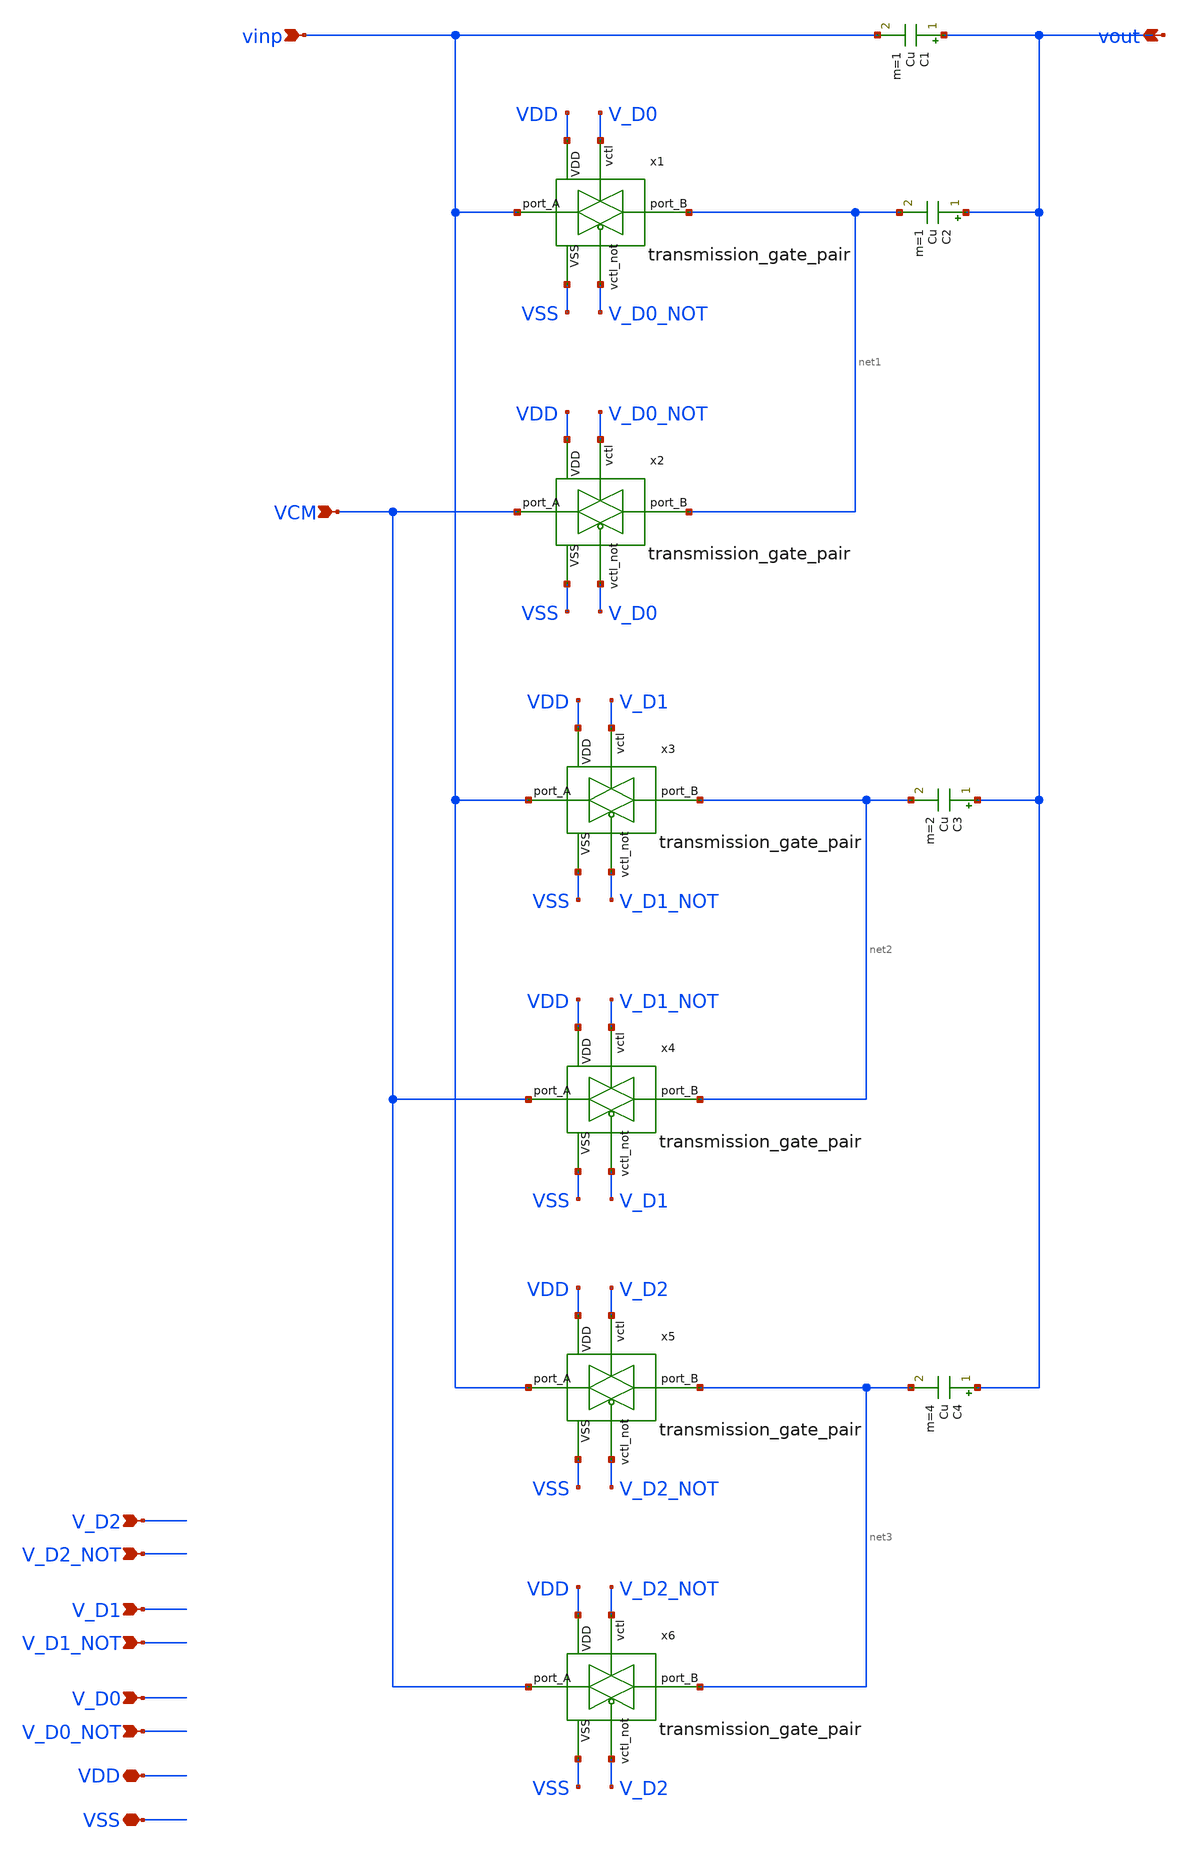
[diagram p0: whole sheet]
** sch_path: analog-db/circuits/sw_003_binary_capbank/pdk/ihp-sg13g2/schematic/capbank.sch
* Copyright 2026 MacAnalog Research Group
**.subckt capbank VDD VSS V_D0 V_D0_NOT V_D1 V_D1_NOT V_D2 V_D2_NOT vinp vout VCM
*.iopin VDD
*.iopin VSS
*.ipin V_D0
*.ipin V_D0_NOT
*.ipin V_D1
*.ipin V_D1_NOT
*.ipin V_D2
*.ipin V_D2_NOT
*.ipin vinp
*.opin vout
*.ipin VCM
C1 vout vinp Cu m=1
C2 vout net1 Cu m=1
x1 V_D0_NOT VDD net1 VSS vinp V_D0 transmission_gate_pair
x2 V_D0 VDD net1 VSS VCM V_D0_NOT transmission_gate_pair
C3 vout net2 Cu m=2
x3 V_D1_NOT VDD net2 VSS vinp V_D1 transmission_gate_pair
x4 V_D1 VDD net2 VSS VCM V_D1_NOT transmission_gate_pair
C4 vout net3 Cu m=4
x5 V_D2_NOT VDD net3 VSS vinp V_D2 transmission_gate_pair
x6 V_D2 VDD net3 VSS VCM V_D2_NOT transmission_gate_pair
**.ends

* expanding   symbol:  shared/transmission_gate_pair.sym # of pins=6
** sym_path: analog-db/drawings/shared/transmission_gate_pair.sym
** sch_path: analog-db/drawings/shared/transmission_gate_pair.sch
.subckt transmission_gate_pair vctl_not VDD port_B VSS port_A vctl
*.ipin port_A
*.ipin port_B
*.ipin vctl
*.ipin VSS
*.ipin VDD
*.ipin vctl_not
XM1 port_A vctl port_B VSS sg13_lv_nmos w=tg_n_w l=tg_n_l ng=1 m=1 mm_ok=1
XM2 port_B vctl_not port_A VDD sg13_lv_pmos w=tg_p_w l=tg_p_l ng=1 m=1 mm_ok=1
.ends

.end
